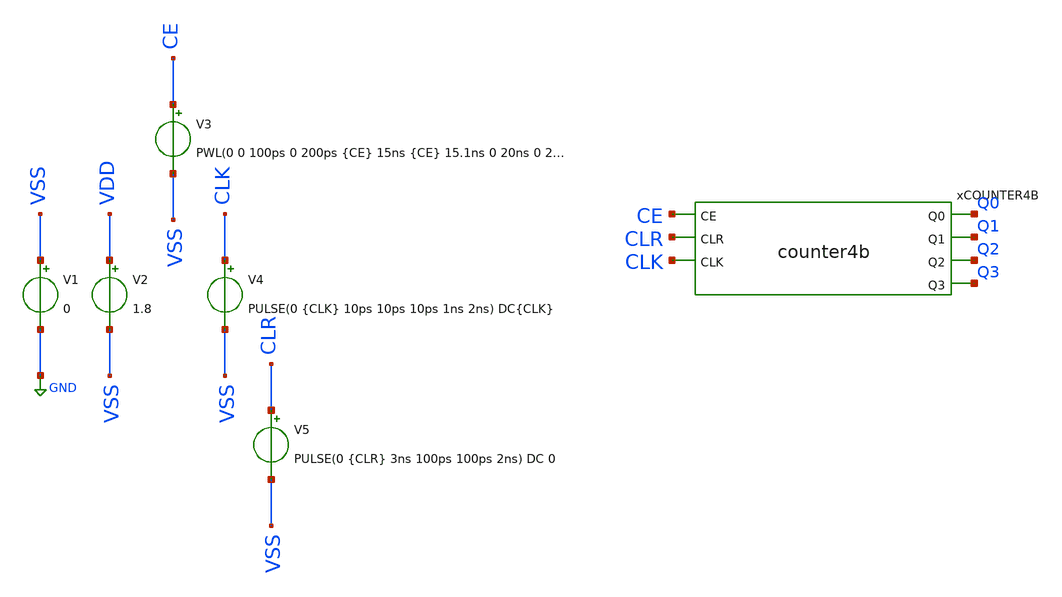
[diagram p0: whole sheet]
** sch_path: track_vlsi/scandaliaris/sch/tb_counter4b.sch
**.subckt tb_counter4b
V1 VSS GND 0
V2 VDD VSS 1.8
V3 CE VSS PWL(0 0 100ps 0 200ps {CE} 15ns {CE} 15.1ns 0 20ns 0 20.1ns {CE} 50ns {CE})
V4 CLK VSS PULSE(0 {CLK} 10ps 10ps 10ps 1ns 2ns) DC{CLK}

V5 CLR VSS PULSE(0 {CLR} 3ns 100ps 100ps 2ns) DC 0
xCOUNTER4B CE Q0 CLR CLK Q1 Q2 Q3 VSS VDD counter4b
**** begin user architecture code


* Parametros del circuito
.param VDD = 1.8
.param CE = 1.8
.param CLK = 1.8
.param CLR = 1.8
.options TEMP = 27.0

* Include
.lib /home/eamta/skywater/skywater-pdk/libraries/sky130_fd_pr_ngspice/latest/models/corners/sky130.lib TT

* Signals to SAVE
.save all
 + @M.X1.XM1.msky130_fd_pr__nfet_01v8[id]
 + @M.X1.XM1.msky130_fd_pr__nfet_01v8[gm]
 + @M.X1.XM2.msky130_fd_pr__pfet_01v8[id]
 + @M.X1.XM2.msky130_fd_pr__pfet_01v8[gm]

* Simulation
.control
  tran .05n 50ns
  setplot tran1
  plot v(Q0) v(Q1)+2 v(Q2)+4 v(Q3)+6 v(CE)+8 v(CLK)+10 v(CLR)+12
  *set plot tran2
  *plot @M.X1.XM1.msky130_fd_pr__nfet_01v8[id] @M.X1.XM2.msky130_fd_pr__pfet_01v8[id]
  *set plot tran3
  *plot @M.X1.XM1.msky130_fd_pr__nfet_01v8[gm] @M.X1.XM2.msky130_fd_pr__pfet_01v8[gm]
  *set filetype=ascii
  write tb_dffc_tran.raw

  reset
  *dc V3 0 1.8 0.01
  *setplot dc1
  *plot v(OUT) v(VINA) v(VINB)
  *write tb_dffc_dc.raw

  *reset
  *op
  *save all
  *write tb_dffc.raw
  *print all
.endc

.end


**** end user architecture code
**.ends
.GLOBAL GND
.end
